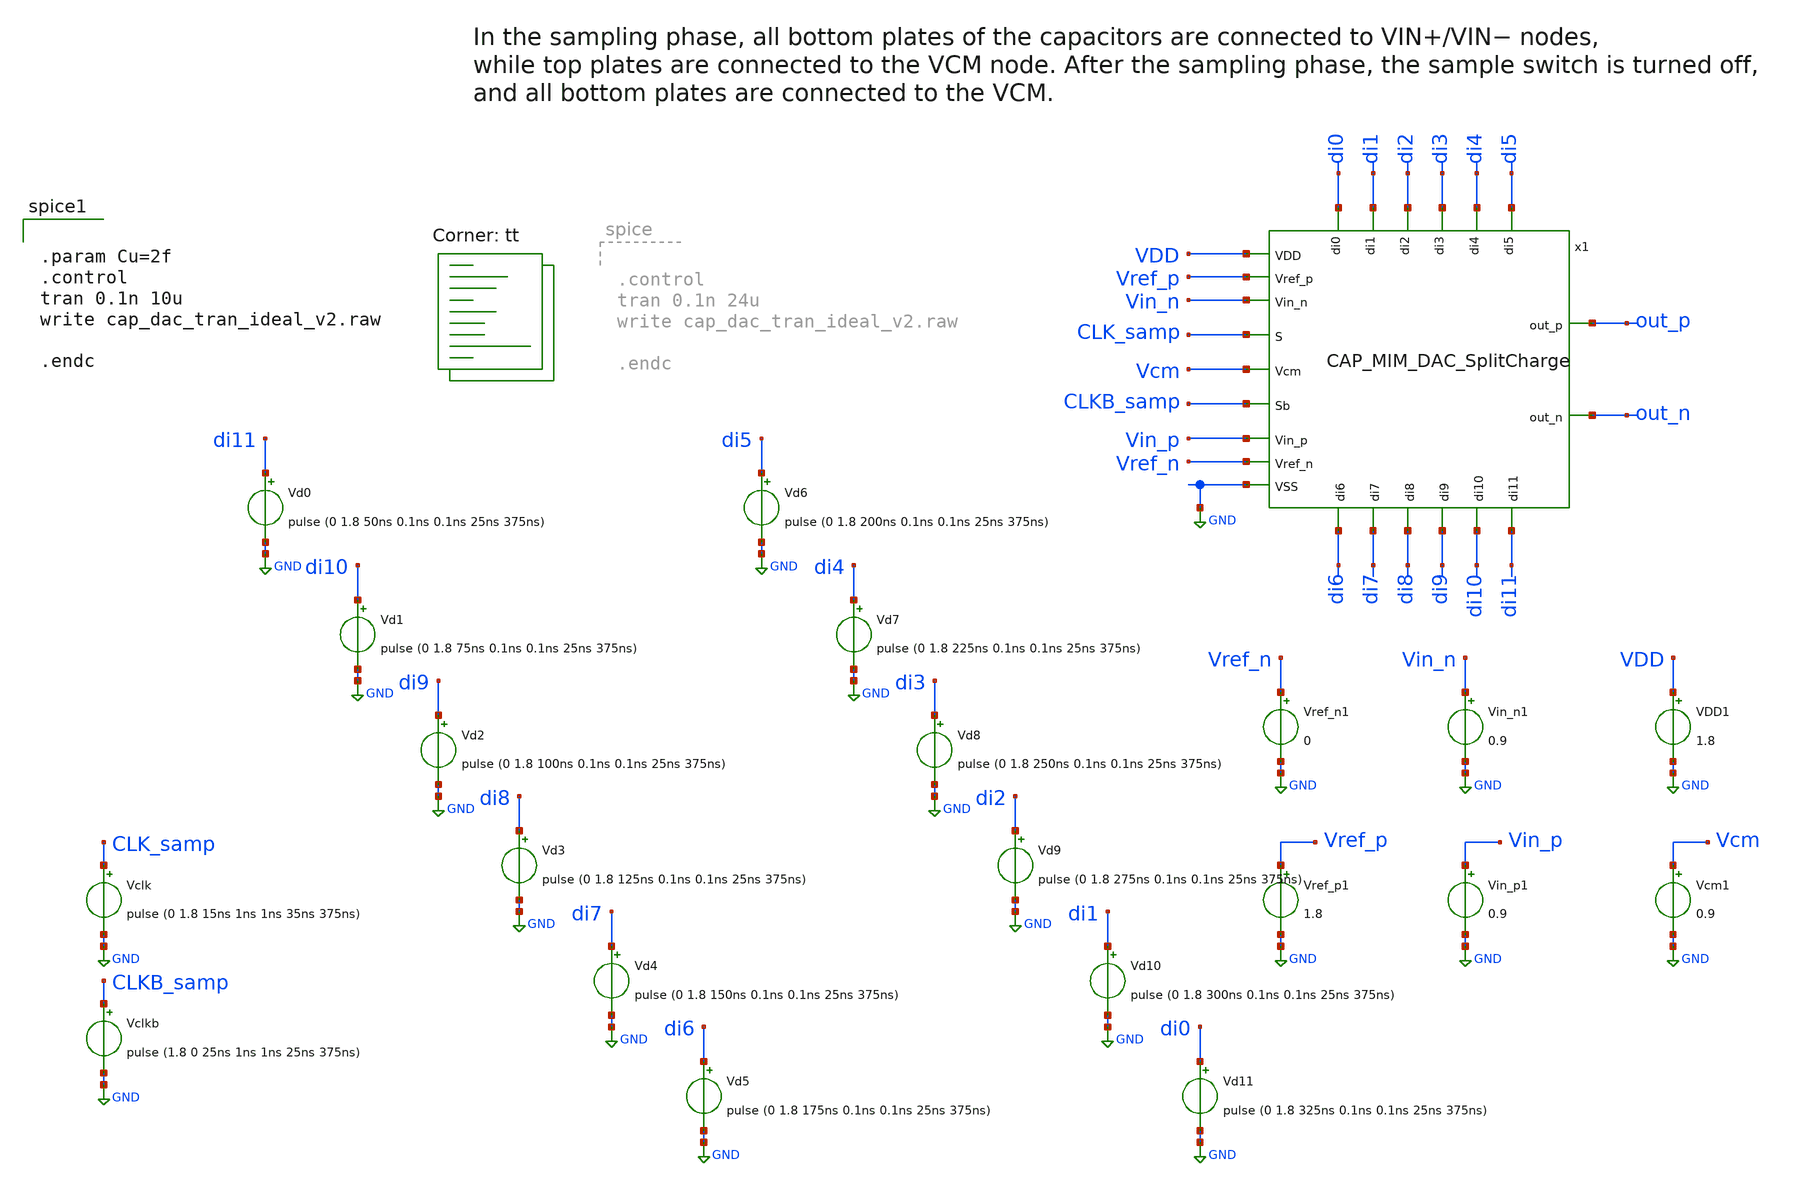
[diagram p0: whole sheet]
** sch_path: CAP_DAC_ideal__tb_v2.sch
**.subckt CAP_DAC_ideal__tb_v2
Vclk CLK_samp GND pulse (0 1.8 15ns 1ns 1ns 35ns 375ns)
Vclkb CLKB_samp GND pulse (1.8 0 25ns 1ns 1ns 25ns 375ns)
Vd0 di11 GND pulse (0 1.8 50ns 0.1ns 0.1ns 25ns 375ns)
Vd1 di10 GND pulse (0 1.8 75ns 0.1ns 0.1ns 25ns 375ns)
Vd2 di9 GND pulse (0 1.8 100ns 0.1ns 0.1ns 25ns 375ns)
Vd3 di8 GND pulse (0 1.8 125ns 0.1ns 0.1ns 25ns 375ns)
Vd4 di7 GND pulse (0 1.8 150ns 0.1ns 0.1ns 25ns 375ns)
Vd5 di6 GND pulse (0 1.8 175ns 0.1ns 0.1ns 25ns 375ns)
Vd6 di5 GND pulse (0 1.8 200ns 0.1ns 0.1ns 25ns 375ns)
Vd7 di4 GND pulse (0 1.8 225ns 0.1ns 0.1ns 25ns 375ns)
Vd8 di3 GND pulse (0 1.8 250ns 0.1ns 0.1ns 25ns 375ns)
Vd9 di2 GND pulse (0 1.8 275ns 0.1ns 0.1ns 25ns 375ns)
Vd10 di1 GND pulse (0 1.8 300ns 0.1ns 0.1ns 25ns 375ns)
Vd11 di0 GND pulse (0 1.8 325ns 0.1ns 0.1ns 25ns 375ns)
VDD1 VDD GND 1.8
Vcm1 Vcm GND 0.9
Vin_n1 Vin_n GND 0.9
Vin_p1 Vin_p GND 0.9
Vref_n1 Vref_n GND 0
Vref_p1 Vref_p GND 1.8
x1 Vref_p Vin_n di0 di1 di2 VDD di3 GND di4 out_p Vcm di5 CLK_samp di6 CLKB_samp di7 out_n di8 di9
+ di10 di11 Vin_p Vref_n CAP_MIM_DAC_SplitCharge
**** begin user architecture code
.lib $::SKYWATER_MODELS/sky130.lib.spice tt


.param Cu=2f
.control
tran 0.1n 10u
write cap_dac_tran_ideal_v2.raw

.endc


**** end user architecture code
**.ends

* expanding   symbol:  Thesis/CAP_MIM_DAC_SplitCharge.sym # of pins=23
** sym_path: CAP_MIM_DAC_SplitCharge.sym
** sch_path: CAP_MIM_DAC_SplitCharge.sch
.subckt CAP_MIM_DAC_SplitCharge Vref_p Vin_n di0 di1 di2 VDD di3 VSS di4 out_p Vcm di5 S di6 Sb di7
+ out_n di8 di9 di10 di11 Vin_p Vref_n
*.ipin VDD
*.ipin VSS
*.ipin S
*.ipin Sb
*.ipin di3
*.ipin Vcm
*.opin out_p
*.opin out_n
*.ipin Vref_p
*.ipin Vref_n
*.ipin di0
*.ipin di1
*.ipin di2
*.ipin di5
*.ipin di4
*.ipin di7
*.ipin di6
*.ipin di9
*.ipin di8
*.ipin di11
*.ipin di10
*.ipin Vin_n
*.ipin Vin_p
x30 VDD Vref_n Vref_p VSS S Sb d11 db11 in_p_sampled net7 Network_Switch
x31 VDD Vref_n Vref_p VSS S Sb d10 db10 in_p_sampled net8 Network_Switch
x32 VDD Vref_n Vref_p VSS S Sb d9 db9 in_p_sampled net9 Network_Switch
x33 VDD Vref_n Vref_p VSS S Sb d8 db8 in_p_sampled net10 Network_Switch
x34 VDD Vref_n Vref_p VSS S Sb d7 db7 in_p_sampled net12 Network_Switch
x35 VDD Vref_n Vref_p VSS S Sb d6 db6 in_p_sampled net11 Network_Switch
x36 VDD Vref_n Vref_p VSS S Sb d5 db5 in_p_sampled net6 Network_Switch
x37 VDD Vref_n Vref_p VSS S Sb d4 db4 in_p_sampled net5 Network_Switch
x38 VDD Vref_n Vref_p VSS S Sb d3 db3 in_p_sampled net4 Network_Switch
x39 VDD Vref_n Vref_p VSS S Sb d2 db2 in_p_sampled net3 Network_Switch
x40 VDD Vref_n Vref_p VSS S Sb d1 db1 in_p_sampled net2 Network_Switch
x41 VDD Vref_n Vref_p VSS S Sb d0 db0 in_p_sampled net1 Network_Switch
x42 VDD Vref_p Vref_n VSS S Sb d11 db11 in_n_sampled net24 Network_Switch
x43 VDD Vref_p Vref_n VSS S Sb d10 db10 in_n_sampled net23 Network_Switch
x44 VDD Vref_p Vref_n VSS S Sb d9 db9 in_n_sampled net22 Network_Switch
x45 VDD Vref_p Vref_n VSS S Sb d8 db8 in_n_sampled net21 Network_Switch
x46 VDD Vref_p Vref_n VSS S Sb d7 db7 in_n_sampled net20 Network_Switch
x47 VDD Vref_p Vref_n VSS S Sb d6 db6 in_n_sampled net19 Network_Switch
x48 VDD Vref_p Vref_n VSS S Sb d5 db5 in_n_sampled net18 Network_Switch
x49 VDD Vref_p Vref_n VSS S Sb d4 db4 in_n_sampled net17 Network_Switch
x50 VDD Vref_p Vref_n VSS S Sb d3 db3 in_n_sampled net16 Network_Switch
x51 VDD Vref_p Vref_n VSS S Sb d2 db2 in_n_sampled net15 Network_Switch
x52 VDD Vref_p Vref_n VSS S Sb d1 db1 in_n_sampled net14 Network_Switch
x53 VDD Vref_p Vref_n VSS S Sb d0 db0 in_n_sampled net13 Network_Switch
x27 out_p Sb S VDD VSS out_n transmission_gate
x2 VDD di0 db0 VSS Inverter
x3 VDD db0 d0 VSS Inverter
x4 VDD di1 db1 VSS Inverter
x5 VDD db1 d1 VSS Inverter
x6 VDD di2 db2 VSS Inverter
x7 VDD db2 d2 VSS Inverter
x8 VDD di3 db3 VSS Inverter
x9 VDD db3 d3 VSS Inverter
x10 VDD di4 db4 VSS Inverter
x11 VDD db4 d4 VSS Inverter
x12 VDD di5 db5 VSS Inverter
x13 VDD db5 d5 VSS Inverter
x14 VDD di6 db6 VSS Inverter
x15 VDD db6 d6 VSS Inverter
x16 VDD di7 db7 VSS Inverter
x17 VDD db7 d7 VSS Inverter
x18 VDD di8 db8 VSS Inverter
x19 VDD db8 d8 VSS Inverter
x20 VDD di9 db9 VSS Inverter
x21 VDD db9 d9 VSS Inverter
x22 VDD di10 db10 VSS Inverter
x23 VDD db10 d10 VSS Inverter
x24 VDD di11 db11 VSS Inverter
x25 VDD db11 d11 VSS Inverter
x28 Vcm Sb S VDD VSS out_p transmission_gate
x29 Vcm Sb S VDD VSS out_n transmission_gate
x56 VDD Vref_p Vref_n VSS S Sb VSS VDD in_n_sampled net26 Network_Switch
x57 VDD Vref_n Vref_p VSS S Sb VSS VDD in_p_sampled net25 Network_Switch
XC16 net20 out_p sky130_fd_pr__cap_mim_m3_1 W=1.198 L=1.198 MF=2 m=2
XC17 net21 out_p sky130_fd_pr__cap_mim_m3_1 W=1.763 L=1.763 MF=2 m=2
XC18 net22 out_p sky130_fd_pr__cap_mim_m3_1 W=2.57 L=2.57 MF=2 m=2
XC19 net23 out_p sky130_fd_pr__cap_mim_m3_1 W=3.705 L=3.705 MF=2 m=2
XC20 net24 out_p sky130_fd_pr__cap_mim_m3_1 W=5.31 L=5.31 MF=2 m=2
x1 VDD Vin_n Sb S in_n_sampled VSS bootstrapped_switch_SH
x26 VDD Vin_p Sb S in_p_sampled VSS bootstrapped_switch_SH
x58 node_n Sb S VDD VSS node_p transmission_gate
x59 Vcm Sb S VDD VSS node_n transmission_gate
x60 Vcm Sb S VDD VSS node_p transmission_gate
XC43 net26 out_p sky130_fd_pr__cap_mim_m3_1 W=0.8 L=0.8 MF=2 m=2
XC21 net19 out_p sky130_fd_pr__cap_mim_m3_1 W=0.8 L=0.8 MF=2 m=2
XC37 out_n net12 sky130_fd_pr__cap_mim_m3_1 W=1.198 L=1.198 MF=2 m=2
XC38 out_n net10 sky130_fd_pr__cap_mim_m3_1 W=1.763 L=1.763 MF=2 m=2
XC39 out_n net9 sky130_fd_pr__cap_mim_m3_1 W=2.57 L=2.57 MF=2 m=2
XC40 out_n net8 sky130_fd_pr__cap_mim_m3_1 W=3.705 L=3.705 MF=2 m=2
XC41 out_n net7 sky130_fd_pr__cap_mim_m3_1 W=5.31 L=5.31 MF=2 m=2
XC42 out_n net25 sky130_fd_pr__cap_mim_m3_1 W=0.8 L=0.8 MF=2 m=2
XC52 out_n net11 sky130_fd_pr__cap_mim_m3_1 W=0.8 L=0.8 MF=2 m=2
XC1 net14 node_n sky130_fd_pr__cap_mim_m3_1 W=1.198 L=1.198 MF=2 m=2
XC8 net15 node_n sky130_fd_pr__cap_mim_m3_1 W=1.763 L=1.763 MF=2 m=2
XC15 net16 node_n sky130_fd_pr__cap_mim_m3_1 W=2.57 L=2.57 MF=2 m=2
XC28 net17 node_n sky130_fd_pr__cap_mim_m3_1 W=3.705 L=3.705 MF=2 m=2
XC29 net18 node_n sky130_fd_pr__cap_mim_m3_1 W=5.31 L=5.31 MF=2 m=2
XC30 net13 node_n sky130_fd_pr__cap_mim_m3_1 W=0.8 L=0.8 MF=2 m=2
XC31 node_p net2 sky130_fd_pr__cap_mim_m3_1 W=1.198 L=1.198 MF=2 m=2
XC32 node_p net3 sky130_fd_pr__cap_mim_m3_1 W=1.763 L=1.763 MF=2 m=2
XC33 node_p net4 sky130_fd_pr__cap_mim_m3_1 W=2.57 L=2.57 MF=2 m=2
XC34 node_p net27 sky130_fd_pr__cap_mim_m3_1 W=3.705 L=3.705 MF=2 m=2
XC35 node_p net28 sky130_fd_pr__cap_mim_m3_1 W=5.31 L=5.31 MF=2 m=2
XC36 node_p net1 sky130_fd_pr__cap_mim_m3_1 W=0.8 L=0.8 MF=2 m=2
XC45 node_n out_p sky130_fd_pr__cap_mim_m3_1 W=0.8 L=0.8 MF=2 m=2
XC46 node_p out_n sky130_fd_pr__cap_mim_m3_1 W=0.8 L=0.8 MF=2 m=2
.ends


* expanding   symbol:  Network_Switch.sym # of pins=10
** sym_path: Network_Switch.sym
** sch_path: Network_Switch.sch
.subckt Network_Switch VDD ground Vref VSS S Sb d db Vin Vout
*.ipin ground
*.ipin Vref
*.ipin Vin
*.opin Vout
*.ipin VDD
*.ipin VSS
*.ipin S
*.ipin Sb
*.ipin d
*.ipin db
x1 ground d db VDD VSS net1 transmission_gate
x2 Vref db d VDD VSS net1 transmission_gate
x3 net1 S Sb VDD VSS Vout transmission_gate
x4 Vin Sb S VDD VSS Vout transmission_gate
.ends


* expanding   symbol:  bootstrapped_switch.sym # of pins=6
** sym_path: bootstrapped_switch.sym
** sch_path: bootstrapped_switch.sch
.subckt bootstrapped_switch VDD in clkb clk out VSS
*.ipin in
*.opin out
*.ipin VSS
*.ipin VDD
*.ipin clkb
*.ipin clk
XM1 net4 clkb net5 net5 sky130_fd_pr__nfet_01v8 L=0.15 W=2 nf=1 ad='int((nf+1)/2) * W/nf * 0.29' as='int((nf+2)/2) * W/nf * 0.29'
+ pd='2*int((nf+1)/2) * (W/nf + 0.29)' ps='2*int((nf+2)/2) * (W/nf + 0.29)' nrd='0.29 / W' nrs='0.29 / W'
+ sa=0 sb=0 sd=0 mult=1 m=1
XM2 in Vg net4 VSS sky130_fd_pr__nfet_01v8 L=1 W=0.5 nf=1 ad='int((nf+1)/2) * W/nf * 0.29' as='int((nf+2)/2) * W/nf * 0.29'
+ pd='2*int((nf+1)/2) * (W/nf + 0.29)' ps='2*int((nf+2)/2) * (W/nf + 0.29)' nrd='0.29 / W' nrs='0.29 / W'
+ sa=0 sb=0 sd=0 mult=1 m=1
XM3 Vp Vg net1 Vp sky130_fd_pr__pfet_01v8 L=0.15 W=2 nf=1 ad='int((nf+1)/2) * W/nf * 0.29' as='int((nf+2)/2) * W/nf * 0.29'
+ pd='2*int((nf+1)/2) * (W/nf + 0.29)' ps='2*int((nf+2)/2) * (W/nf + 0.29)' nrd='0.29 / W' nrs='0.29 / W'
+ sa=0 sb=0 sd=0 mult=1 m=1
XM5 out Vg in VSS sky130_fd_pr__nfet_01v8 L=0.15 W=30 nf=1 ad='int((nf+1)/2) * W/nf * 0.29' as='int((nf+2)/2) * W/nf * 0.29'
+ pd='2*int((nf+1)/2) * (W/nf + 0.29)' ps='2*int((nf+2)/2) * (W/nf + 0.29)' nrd='0.29 / W' nrs='0.29 / W'
+ sa=0 sb=0 sd=0 mult=1 m=1
XM6 out clkb in VDD sky130_fd_pr__pfet_01v8 L=0.15 W=30 nf=1 ad='int((nf+1)/2) * W/nf * 0.29' as='int((nf+2)/2) * W/nf * 0.29'
+ pd='2*int((nf+1)/2) * (W/nf + 0.29)' ps='2*int((nf+2)/2) * (W/nf + 0.29)' nrd='0.29 / W' nrs='0.29 / W'
+ sa=0 sb=0 sd=0 mult=1 m=1
XM8 net6 clkb net2 net2 sky130_fd_pr__nfet_01v8 L=0.15 W=0.5 nf=1 ad='int((nf+1)/2) * W/nf * 0.29' as='int((nf+2)/2) * W/nf * 0.29'
+ pd='2*int((nf+1)/2) * (W/nf + 0.29)' ps='2*int((nf+2)/2) * (W/nf + 0.29)' nrd='0.29 / W' nrs='0.29 / W'
+ sa=0 sb=0 sd=0 mult=1 m=1
XC1 net4 Vp sky130_fd_pr__cap_mim_m3_1 W=18 L=18 MF=10 m=10
XM7 Vg VDD net6 net6 sky130_fd_pr__nfet_01v8 L=0.15 W=0.5 nf=1 ad='int((nf+1)/2) * W/nf * 0.29' as='int((nf+2)/2) * W/nf * 0.29'
+ pd='2*int((nf+1)/2) * (W/nf + 0.29)' ps='2*int((nf+2)/2) * (W/nf + 0.29)' nrd='0.29 / W' nrs='0.29 / W'
+ sa=0 sb=0 sd=0 mult=1 m=1
XM4 Vg net3 Vp Vp sky130_fd_pr__pfet_01v8 L=0.15 W=0.5 nf=1 ad='int((nf+1)/2) * W/nf * 0.29' as='int((nf+2)/2) * W/nf * 0.29'
+ pd='2*int((nf+1)/2) * (W/nf + 0.29)' ps='2*int((nf+2)/2) * (W/nf + 0.29)' nrd='0.29 / W' nrs='0.29 / W'
+ sa=0 sb=0 sd=0 mult=1 m=1
XC2 out VSS sky130_fd_pr__cap_mim_m3_1 W=36 L=36 MF=20 m=20
XM10 net1 clk net7 net1 sky130_fd_pr__pfet_01v8 L=0.15 W=2 nf=1 ad='int((nf+1)/2) * W/nf * 0.29' as='int((nf+2)/2) * W/nf * 0.29'
+ pd='2*int((nf+1)/2) * (W/nf + 0.29)' ps='2*int((nf+2)/2) * (W/nf + 0.29)' nrd='0.29 / W' nrs='0.29 / W'
+ sa=0 sb=0 sd=0 mult=1 m=1
XM11 net5 clkb net8 net8 sky130_fd_pr__nfet_01v8 L=0.15 W=2 nf=1 ad='int((nf+1)/2) * W/nf * 0.29' as='int((nf+2)/2) * W/nf * 0.29'
+ pd='2*int((nf+1)/2) * (W/nf + 0.29)' ps='2*int((nf+2)/2) * (W/nf + 0.29)' nrd='0.29 / W' nrs='0.29 / W'
+ sa=0 sb=0 sd=0 mult=1 m=1
XM12 net7 clk VDD net7 sky130_fd_pr__pfet_01v8 L=0.15 W=2 nf=1 ad='int((nf+1)/2) * W/nf * 0.29' as='int((nf+2)/2) * W/nf * 0.29'
+ pd='2*int((nf+1)/2) * (W/nf + 0.29)' ps='2*int((nf+2)/2) * (W/nf + 0.29)' nrd='0.29 / W' nrs='0.29 / W'
+ sa=0 sb=0 sd=0 mult=1 m=1
XM13 net8 clkb VSS VSS sky130_fd_pr__nfet_01v8 L=0.15 W=2 nf=1 ad='int((nf+1)/2) * W/nf * 0.29' as='int((nf+2)/2) * W/nf * 0.29'
+ pd='2*int((nf+1)/2) * (W/nf + 0.29)' ps='2*int((nf+2)/2) * (W/nf + 0.29)' nrd='0.29 / W' nrs='0.29 / W'
+ sa=0 sb=0 sd=0 mult=1 m=1
XM14 net2 clkb VSS VSS sky130_fd_pr__nfet_01v8 L=0.15 W=0.5 nf=1 ad='int((nf+1)/2) * W/nf * 0.29' as='int((nf+2)/2) * W/nf * 0.29'
+ pd='2*int((nf+1)/2) * (W/nf + 0.29)' ps='2*int((nf+2)/2) * (W/nf + 0.29)' nrd='0.29 / W' nrs='0.29 / W'
+ sa=0 sb=0 sd=0 mult=1 m=1
XM15 net3 clk VDD VDD sky130_fd_pr__pfet_01v8 L=0.15 W=1 nf=1 ad='int((nf+1)/2) * W/nf * 0.29' as='int((nf+2)/2) * W/nf * 0.29'
+ pd='2*int((nf+1)/2) * (W/nf + 0.29)' ps='2*int((nf+2)/2) * (W/nf + 0.29)' nrd='0.29 / W' nrs='0.29 / W'
+ sa=0 sb=0 sd=0 mult=1 m=1
XM16 net3 clk net4 VSS sky130_fd_pr__nfet_01v8 L=1 W=0.5 nf=1 ad='int((nf+1)/2) * W/nf * 0.29' as='int((nf+2)/2) * W/nf * 0.29'
+ pd='2*int((nf+1)/2) * (W/nf + 0.29)' ps='2*int((nf+2)/2) * (W/nf + 0.29)' nrd='0.29 / W' nrs='0.29 / W'
+ sa=0 sb=0 sd=0 mult=1 m=1
XM17 net3 Vg net4 VSS sky130_fd_pr__nfet_01v8 L=0.15 W=2 nf=1 ad='int((nf+1)/2) * W/nf * 0.29' as='int((nf+2)/2) * W/nf * 0.29'
+ pd='2*int((nf+1)/2) * (W/nf + 0.29)' ps='2*int((nf+2)/2) * (W/nf + 0.29)' nrd='0.29 / W' nrs='0.29 / W'
+ sa=0 sb=0 sd=0 mult=1 m=1
.ends


* expanding   symbol:  transmission_gate.sym # of pins=6
** sym_path: transmission_gate.sym
** sch_path: transmission_gate.sch
.subckt transmission_gate in clkb clk VDD VSS out
*.ipin in
*.ipin clk
*.ipin clkb
*.opin out
*.ipin VDD
*.ipin VSS
XM1 out clk in VSS sky130_fd_pr__nfet_01v8 L=0.15 W=0.5 nf=1 ad='int((nf+1)/2) * W/nf * 0.29' as='int((nf+2)/2) * W/nf * 0.29'
+ pd='2*int((nf+1)/2) * (W/nf + 0.29)' ps='2*int((nf+2)/2) * (W/nf + 0.29)' nrd='0.29 / W' nrs='0.29 / W'
+ sa=0 sb=0 sd=0 mult=1 m=1
XM2 out clkb in VDD sky130_fd_pr__pfet_01v8 L=0.15 W=0.5 nf=1 ad='int((nf+1)/2) * W/nf * 0.29' as='int((nf+2)/2) * W/nf * 0.29'
+ pd='2*int((nf+1)/2) * (W/nf + 0.29)' ps='2*int((nf+2)/2) * (W/nf + 0.29)' nrd='0.29 / W' nrs='0.29 / W'
+ sa=0 sb=0 sd=0 mult=1 m=1
.ends


* expanding   symbol:  Inverter.sym # of pins=4
** sym_path: Inverter.sym
** sch_path: Inverter.sch
.subckt Inverter VDD IN OUT VSS
*.ipin IN
*.ipin VSS
*.ipin VDD
*.opin OUT
XM1 OUT IN VSS VSS sky130_fd_pr__nfet_01v8 L=0.3 W=1 nf=1 ad='int((nf+1)/2) * W/nf * 0.29' as='int((nf+2)/2) * W/nf * 0.29'
+ pd='2*int((nf+1)/2) * (W/nf + 0.29)' ps='2*int((nf+2)/2) * (W/nf + 0.29)' nrd='0.29 / W' nrs='0.29 / W'
+ sa=0 sb=0 sd=0 mult=1 m=1
XM2 OUT IN VDD VDD sky130_fd_pr__pfet_01v8 L=0.3 W=2 nf=1 ad='int((nf+1)/2) * W/nf * 0.29' as='int((nf+2)/2) * W/nf * 0.29'
+ pd='2*int((nf+1)/2) * (W/nf + 0.29)' ps='2*int((nf+2)/2) * (W/nf + 0.29)' nrd='0.29 / W' nrs='0.29 / W'
+ sa=0 sb=0 sd=0 mult=1 m=1
.ends


* expanding   symbol:  bootstrapped_switch_SH.sym # of pins=6
** sym_path: bootstrapped_switch_SH.sym
** sch_path: bootstrapped_switch_SH.sch
.subckt bootstrapped_switch_SH VDD in clkb clk out VSS
*.ipin in
*.opin out
*.ipin VSS
*.ipin VDD
*.ipin clkb
*.ipin clk
XM1 net3 clkb net4 net4 sky130_fd_pr__nfet_01v8 L=0.15 W=2 nf=1 ad='int((nf+1)/2) * W/nf * 0.29' as='int((nf+2)/2) * W/nf * 0.29'
+ pd='2*int((nf+1)/2) * (W/nf + 0.29)' ps='2*int((nf+2)/2) * (W/nf + 0.29)' nrd='0.29 / W' nrs='0.29 / W'
+ sa=0 sb=0 sd=0 mult=1 m=1
XM2 in Vg net3 VSS sky130_fd_pr__nfet_01v8 L=1 W=0.5 nf=1 ad='int((nf+1)/2) * W/nf * 0.29' as='int((nf+2)/2) * W/nf * 0.29'
+ pd='2*int((nf+1)/2) * (W/nf + 0.29)' ps='2*int((nf+2)/2) * (W/nf + 0.29)' nrd='0.29 / W' nrs='0.29 / W'
+ sa=0 sb=0 sd=0 mult=1 m=1
XM3 Vp Vg net1 Vp sky130_fd_pr__pfet_01v8 L=0.15 W=2 nf=1 ad='int((nf+1)/2) * W/nf * 0.29' as='int((nf+2)/2) * W/nf * 0.29'
+ pd='2*int((nf+1)/2) * (W/nf + 0.29)' ps='2*int((nf+2)/2) * (W/nf + 0.29)' nrd='0.29 / W' nrs='0.29 / W'
+ sa=0 sb=0 sd=0 mult=1 m=1
XM5 out Vg in VSS sky130_fd_pr__nfet_01v8 L=0.15 W=30 nf=1 ad='int((nf+1)/2) * W/nf * 0.29' as='int((nf+2)/2) * W/nf * 0.29'
+ pd='2*int((nf+1)/2) * (W/nf + 0.29)' ps='2*int((nf+2)/2) * (W/nf + 0.29)' nrd='0.29 / W' nrs='0.29 / W'
+ sa=0 sb=0 sd=0 mult=1 m=1
XM6 out clkb in VDD sky130_fd_pr__pfet_01v8 L=0.15 W=30 nf=1 ad='int((nf+1)/2) * W/nf * 0.29' as='int((nf+2)/2) * W/nf * 0.29'
+ pd='2*int((nf+1)/2) * (W/nf + 0.29)' ps='2*int((nf+2)/2) * (W/nf + 0.29)' nrd='0.29 / W' nrs='0.29 / W'
+ sa=0 sb=0 sd=0 mult=1 m=1
XM8 net5 clkb net2 net2 sky130_fd_pr__nfet_01v8 L=0.15 W=0.5 nf=1 ad='int((nf+1)/2) * W/nf * 0.29' as='int((nf+2)/2) * W/nf * 0.29'
+ pd='2*int((nf+1)/2) * (W/nf + 0.29)' ps='2*int((nf+2)/2) * (W/nf + 0.29)' nrd='0.29 / W' nrs='0.29 / W'
+ sa=0 sb=0 sd=0 mult=1 m=1
XCb net3 Vp sky130_fd_pr__cap_mim_m3_1 W=18 L=18 MF=10 m=10
XM7 Vg VDD net5 net5 sky130_fd_pr__nfet_01v8 L=0.15 W=0.5 nf=1 ad='int((nf+1)/2) * W/nf * 0.29' as='int((nf+2)/2) * W/nf * 0.29'
+ pd='2*int((nf+1)/2) * (W/nf + 0.29)' ps='2*int((nf+2)/2) * (W/nf + 0.29)' nrd='0.29 / W' nrs='0.29 / W'
+ sa=0 sb=0 sd=0 mult=1 m=1
XM4 Vg clkb Vp Vp sky130_fd_pr__pfet_01v8 L=0.15 W=0.5 nf=1 ad='int((nf+1)/2) * W/nf * 0.29' as='int((nf+2)/2) * W/nf * 0.29'
+ pd='2*int((nf+1)/2) * (W/nf + 0.29)' ps='2*int((nf+2)/2) * (W/nf + 0.29)' nrd='0.29 / W' nrs='0.29 / W'
+ sa=0 sb=0 sd=0 mult=1 m=1
XM10 net1 clk net6 net1 sky130_fd_pr__pfet_01v8 L=0.15 W=2 nf=1 ad='int((nf+1)/2) * W/nf * 0.29' as='int((nf+2)/2) * W/nf * 0.29'
+ pd='2*int((nf+1)/2) * (W/nf + 0.29)' ps='2*int((nf+2)/2) * (W/nf + 0.29)' nrd='0.29 / W' nrs='0.29 / W'
+ sa=0 sb=0 sd=0 mult=1 m=1
XM11 net4 clkb net7 net7 sky130_fd_pr__nfet_01v8 L=0.15 W=2 nf=1 ad='int((nf+1)/2) * W/nf * 0.29' as='int((nf+2)/2) * W/nf * 0.29'
+ pd='2*int((nf+1)/2) * (W/nf + 0.29)' ps='2*int((nf+2)/2) * (W/nf + 0.29)' nrd='0.29 / W' nrs='0.29 / W'
+ sa=0 sb=0 sd=0 mult=1 m=1
XM12 net6 clk VDD net6 sky130_fd_pr__pfet_01v8 L=0.15 W=2 nf=1 ad='int((nf+1)/2) * W/nf * 0.29' as='int((nf+2)/2) * W/nf * 0.29'
+ pd='2*int((nf+1)/2) * (W/nf + 0.29)' ps='2*int((nf+2)/2) * (W/nf + 0.29)' nrd='0.29 / W' nrs='0.29 / W'
+ sa=0 sb=0 sd=0 mult=1 m=1
XM13 net7 clkb VSS VSS sky130_fd_pr__nfet_01v8 L=0.15 W=2 nf=1 ad='int((nf+1)/2) * W/nf * 0.29' as='int((nf+2)/2) * W/nf * 0.29'
+ pd='2*int((nf+1)/2) * (W/nf + 0.29)' ps='2*int((nf+2)/2) * (W/nf + 0.29)' nrd='0.29 / W' nrs='0.29 / W'
+ sa=0 sb=0 sd=0 mult=1 m=1
XM14 net2 clkb VSS VSS sky130_fd_pr__nfet_01v8 L=0.15 W=0.5 nf=1 ad='int((nf+1)/2) * W/nf * 0.29' as='int((nf+2)/2) * W/nf * 0.29'
+ pd='2*int((nf+1)/2) * (W/nf + 0.29)' ps='2*int((nf+2)/2) * (W/nf + 0.29)' nrd='0.29 / W' nrs='0.29 / W'
+ sa=0 sb=0 sd=0 mult=1 m=1
XC2 out VSS sky130_fd_pr__cap_mim_m3_1 W=36 L=36 MF=20 m=20
.ends

.GLOBAL GND
.end
